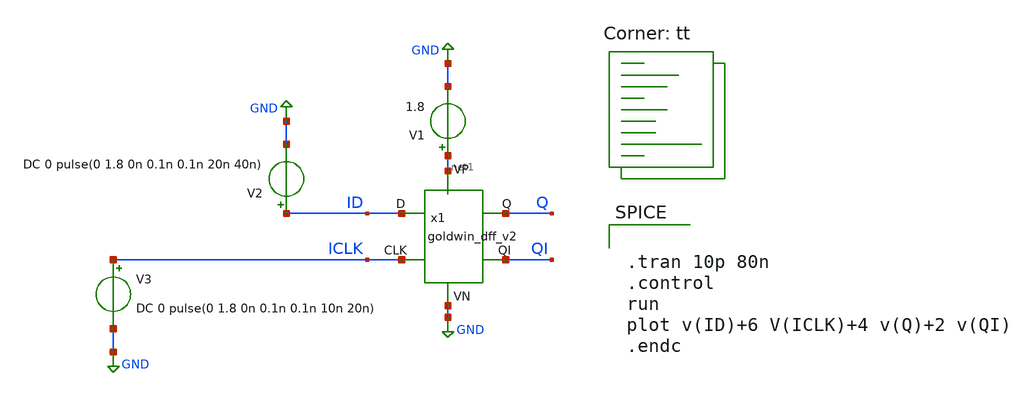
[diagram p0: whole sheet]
** sch_path: APIC-UTS/schematic/goldwin_dff_v2/tb_goldwin_dff_v2.sch
**.subckt tb_goldwin_dff_v2
V1 net1 GND 1.8
V2 ID GND DC 0 pulse(0 1.8 0n 0.1n 0.1n 20n 40n)
V3 ICLK GND DC 0 pulse(0 1.8 0n 0.1n 0.1n 10n 20n)
x1 ID ICLK net1 GND Q QI net1 GND goldwin_dff_v2
**** begin user architecture code


.tran 10p 80n
.control
run
plot v(ID)+6 V(ICLK)+4 v(Q)+2 v(QI)
.endc


.lib $::SKYWATER_MODELS/sky130.lib.spice tt
**** end user architecture code
**.ends
.GLOBAL GND
.end
